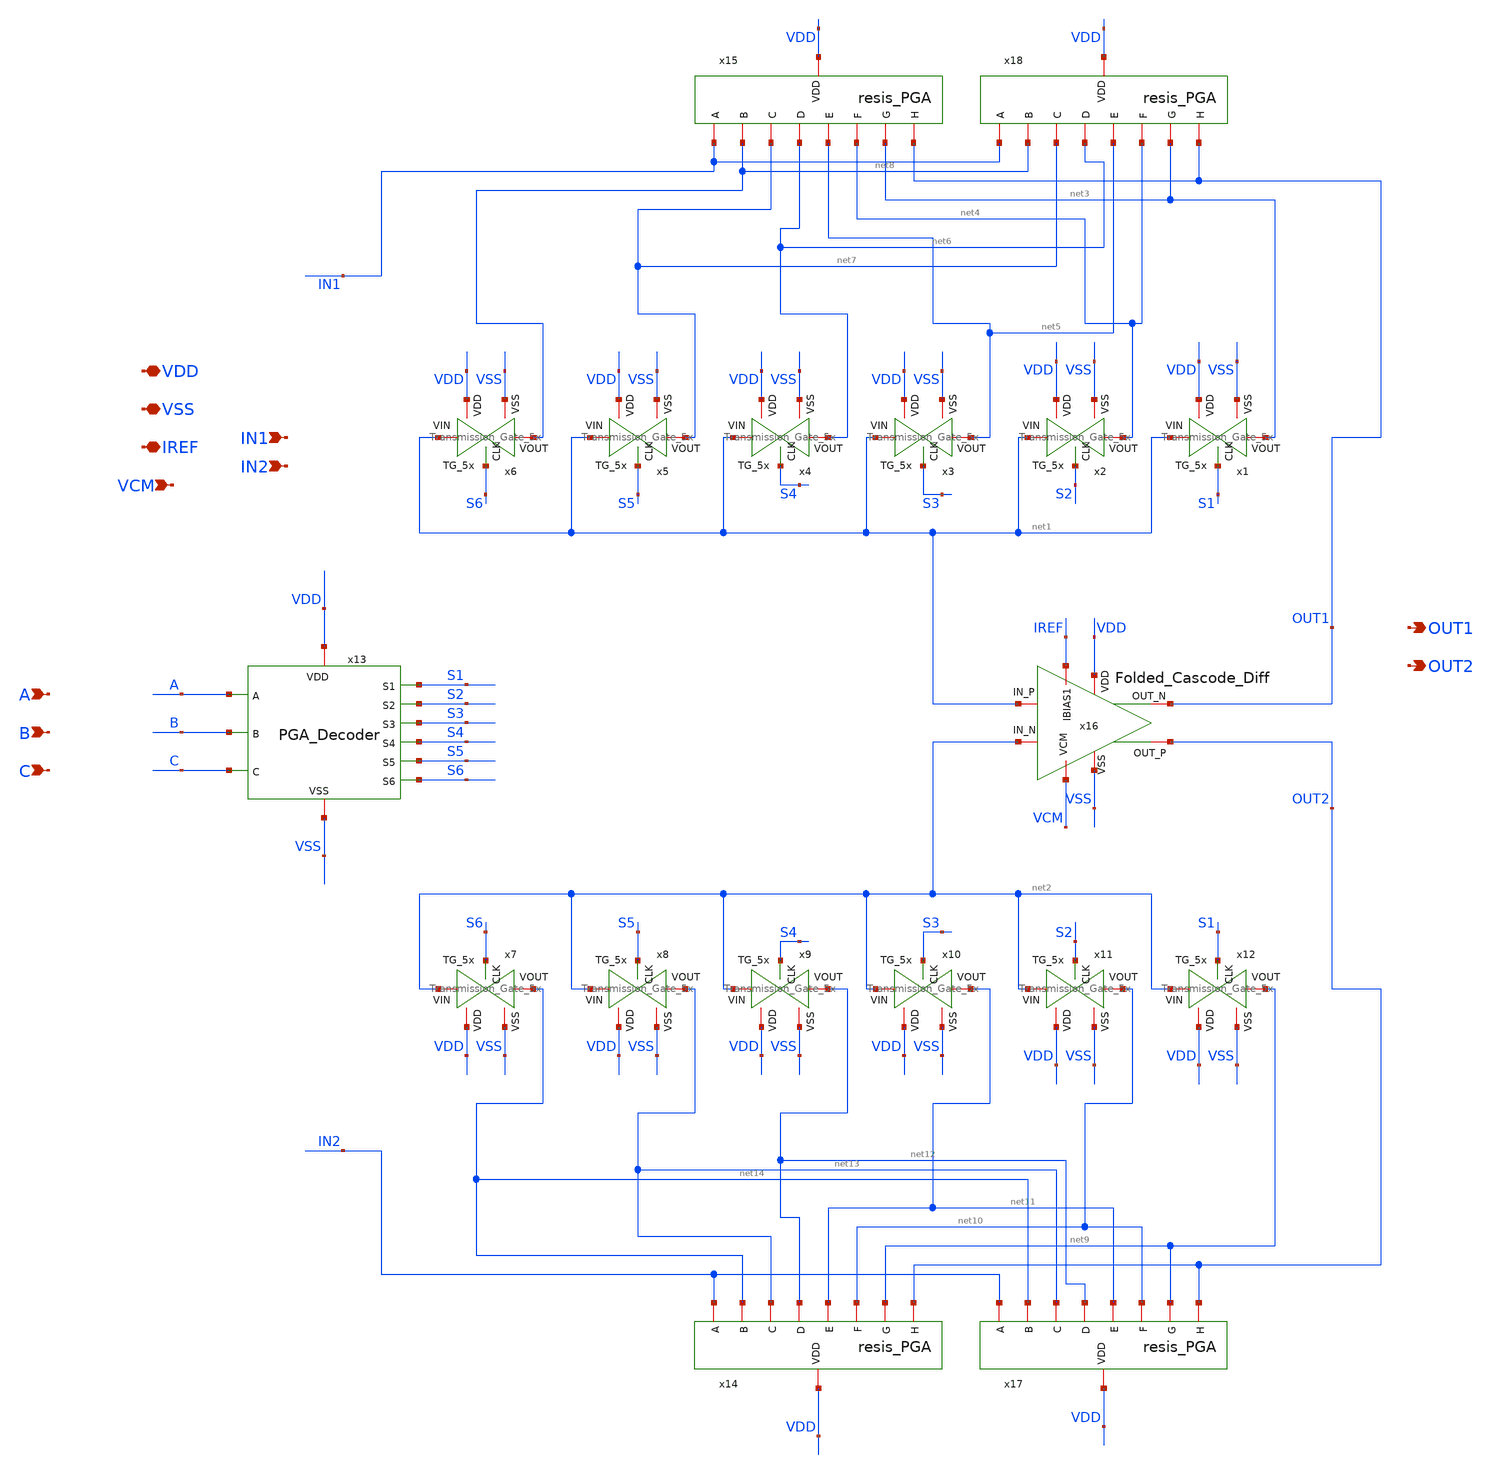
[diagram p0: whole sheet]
** sch_path: SCOP_INPUT_AND_MUX_PAKISTAN_03/Xschem/PGA_block_new/PGA_block_ppoly.sch
**.subckt PGA_block_ppoly A B C VDD VSS IREF VCM OUT1 OUT2 IN1 IN2
*.ipin A
*.ipin B
*.ipin C
*.iopin VDD
*.iopin VSS
*.iopin IREF
*.ipin VCM
*.opin OUT1
*.opin OUT2
*.ipin IN1
*.ipin IN2
x14 VDD IN2 net11 net10 net14 net13 net9 OUT2 net12 resis_PGA
x15 VDD IN1 net5 net4 net8 net7 net3 OUT1 net6 resis_PGA
x17 VDD IN2 net11 net10 net14 net13 net9 OUT2 net12 resis_PGA
x18 VDD IN1 net5 net4 net8 net7 net3 OUT1 net6 resis_PGA
x1 VDD VSS S1 net3 net1 Transmission_Gate_5x
x2 VDD VSS S2 net4 net1 Transmission_Gate_5x
x3 VDD VSS S3 net5 net1 Transmission_Gate_5x
x4 VDD VSS S4 net6 net1 Transmission_Gate_5x
x5 VDD VSS S5 net7 net1 Transmission_Gate_5x
x6 VDD VSS S6 net8 net1 Transmission_Gate_5x
x7 VDD VSS S6 net14 net2 Transmission_Gate_5x
x8 VDD VSS S5 net13 net2 Transmission_Gate_5x
x9 VDD VSS S4 net12 net2 Transmission_Gate_5x
x10 VDD VSS S3 net11 net2 Transmission_Gate_5x
x11 VDD VSS S2 net10 net2 Transmission_Gate_5x
x12 VDD VSS S1 net9 net2 Transmission_Gate_5x
x16 VDD VSS VCM net2 net1 OUT1 OUT2 IREF Folded_Cascode_Diff
x13 S2 S3 S1 VDD A S6 B S4 C VSS S5 PGA_Decoder
**.ends
.end
